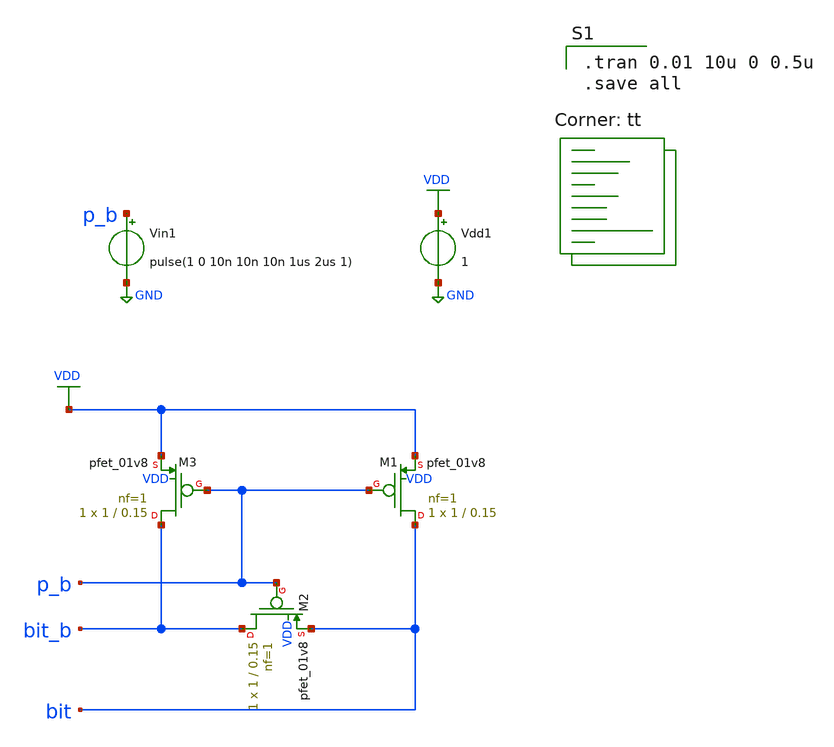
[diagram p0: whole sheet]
** sch_path: gates/Memory/precharge circuit sim.sch
**.subckt precharge circuit sim
XM1 bit p_b VDD VDD sky130_fd_pr__pfet_01v8 L=0.15 W=1 nf=1 ad='int((nf+1)/2) * W/nf * 0.29' as='int((nf+2)/2) * W/nf * 0.29'
+ pd='2*int((nf+1)/2) * (W/nf + 0.29)' ps='2*int((nf+2)/2) * (W/nf + 0.29)' nrd='0.29 / W' nrs='0.29 / W'
+ sa=0 sb=0 sd=0 mult=1 m=1
XM2 bit_b p_b bit VDD sky130_fd_pr__pfet_01v8 L=0.15 W=1 nf=1 ad='int((nf+1)/2) * W/nf * 0.29' as='int((nf+2)/2) * W/nf * 0.29'
+ pd='2*int((nf+1)/2) * (W/nf + 0.29)' ps='2*int((nf+2)/2) * (W/nf + 0.29)' nrd='0.29 / W' nrs='0.29 / W'
+ sa=0 sb=0 sd=0 mult=1 m=1
XM3 bit_b p_b VDD VDD sky130_fd_pr__pfet_01v8 L=0.15 W=1 nf=1 ad='int((nf+1)/2) * W/nf * 0.29' as='int((nf+2)/2) * W/nf * 0.29'
+ pd='2*int((nf+1)/2) * (W/nf + 0.29)' ps='2*int((nf+2)/2) * (W/nf + 0.29)' nrd='0.29 / W' nrs='0.29 / W'
+ sa=0 sb=0 sd=0 mult=1 m=1
Vdd1 VDD GND 1
Vin1 p_b GND pulse(1 0 10n 10n 10n 1us 2us 1)
**** begin user architecture code

.tran 0.01 10u 0 0.5u
.save all

.lib $::SKYWATER_MODELS/sky130.lib.spice tt
**** end user architecture code
**.ends
.GLOBAL VDD
.GLOBAL GND
.end
